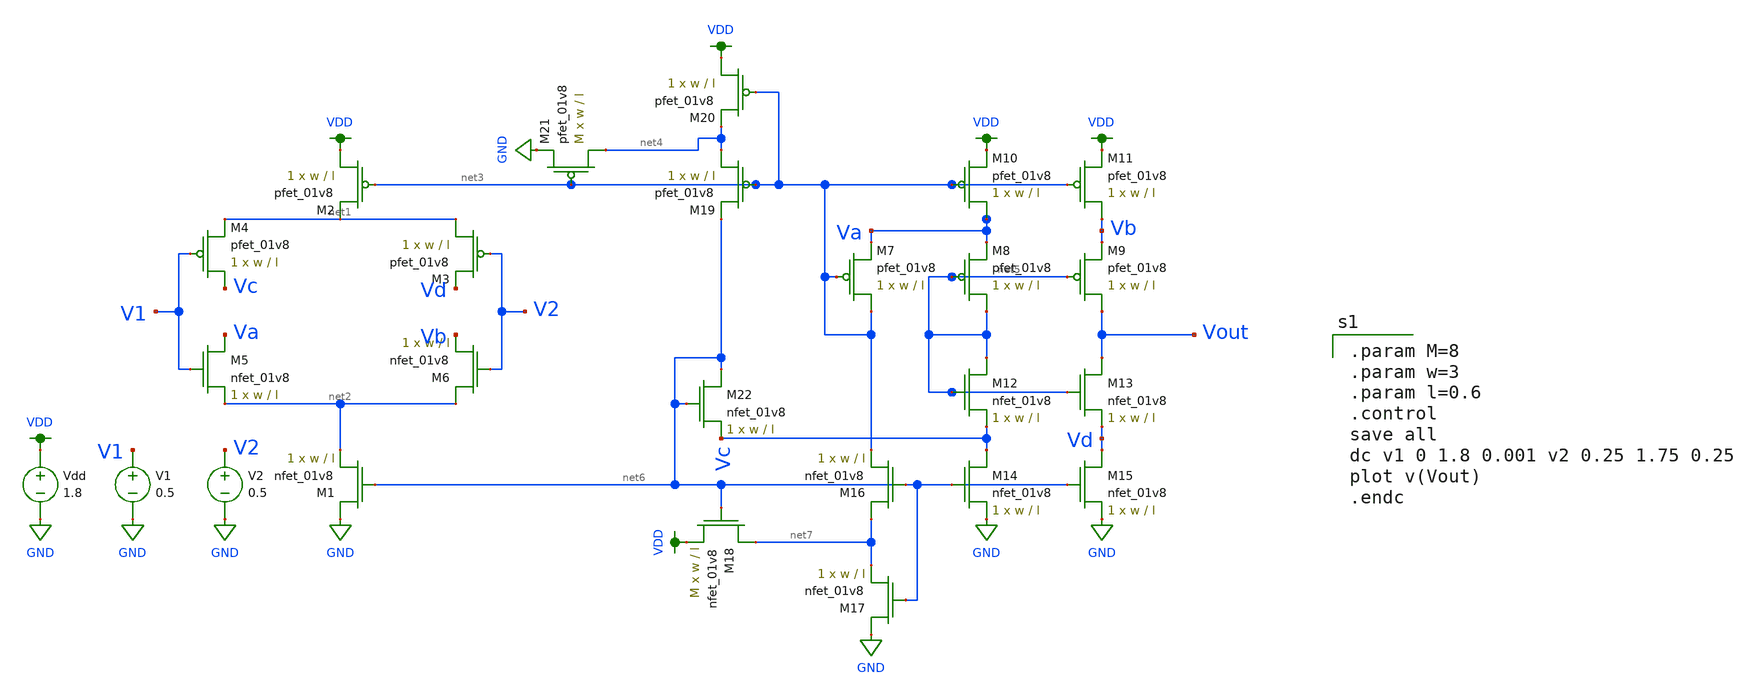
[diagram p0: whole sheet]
** sch_path: brad_circuit.sch
**.subckt brad_circuit
XM1 GND net6 net2 GND sky130_fd_pr__nfet_01v8 L=l W=w nf=1 ad='int((nf+1)/2) * W/nf * 0.29' as='int((nf+2)/2) * W/nf * 0.29'
+ pd='2*int((nf+1)/2) * (W/nf + 0.29)' ps='2*int((nf+2)/2) * (W/nf + 0.29)' nrd='0.29 / W' nrs='0.29 / W'
+ sa=0 sb=0 sd=0 mult=1 m=1
XM2 VDD net3 net1 VDD sky130_fd_pr__pfet_01v8 L=l W=w nf=1 ad='int((nf+1)/2) * W/nf * 0.29' as='int((nf+2)/2) * W/nf * 0.29'
+ pd='2*int((nf+1)/2) * (W/nf + 0.29)' ps='2*int((nf+2)/2) * (W/nf + 0.29)' nrd='0.29 / W' nrs='0.29 / W'
+ sa=0 sb=0 sd=0 mult=1 m=1
XM3 net1 V2 Vd VDD sky130_fd_pr__pfet_01v8 L=l W=w nf=1 ad='int((nf+1)/2) * W/nf * 0.29' as='int((nf+2)/2) * W/nf * 0.29'
+ pd='2*int((nf+1)/2) * (W/nf + 0.29)' ps='2*int((nf+2)/2) * (W/nf + 0.29)' nrd='0.29 / W' nrs='0.29 / W'
+ sa=0 sb=0 sd=0 mult=1 m=1
XM4 Vc V1 net1 VDD sky130_fd_pr__pfet_01v8 L=l W=w nf=1 ad='int((nf+1)/2) * W/nf * 0.29' as='int((nf+2)/2) * W/nf * 0.29'
+ pd='2*int((nf+1)/2) * (W/nf + 0.29)' ps='2*int((nf+2)/2) * (W/nf + 0.29)' nrd='0.29 / W' nrs='0.29 / W'
+ sa=0 sb=0 sd=0 mult=1 m=1
XM5 Va V1 net2 GND sky130_fd_pr__nfet_01v8 L=l W=w nf=1 ad='int((nf+1)/2) * W/nf * 0.29' as='int((nf+2)/2) * W/nf * 0.29'
+ pd='2*int((nf+1)/2) * (W/nf + 0.29)' ps='2*int((nf+2)/2) * (W/nf + 0.29)' nrd='0.29 / W' nrs='0.29 / W'
+ sa=0 sb=0 sd=0 mult=1 m=1
XM6 net2 V2 Vb GND sky130_fd_pr__nfet_01v8 L=l W=w nf=1 ad='int((nf+1)/2) * W/nf * 0.29' as='int((nf+2)/2) * W/nf * 0.29'
+ pd='2*int((nf+1)/2) * (W/nf + 0.29)' ps='2*int((nf+2)/2) * (W/nf + 0.29)' nrd='0.29 / W' nrs='0.29 / W'
+ sa=0 sb=0 sd=0 mult=1 m=1
XM7 net3 net3 Va VDD sky130_fd_pr__pfet_01v8 L=l W=w nf=1 ad='int((nf+1)/2) * W/nf * 0.29' as='int((nf+2)/2) * W/nf * 0.29'
+ pd='2*int((nf+1)/2) * (W/nf + 0.29)' ps='2*int((nf+2)/2) * (W/nf + 0.29)' nrd='0.29 / W' nrs='0.29 / W'
+ sa=0 sb=0 sd=0 mult=1 m=1
XM8 net5 net5 Va VDD sky130_fd_pr__pfet_01v8 L=l W=w nf=1 ad='int((nf+1)/2) * W/nf * 0.29' as='int((nf+2)/2) * W/nf * 0.29'
+ pd='2*int((nf+1)/2) * (W/nf + 0.29)' ps='2*int((nf+2)/2) * (W/nf + 0.29)' nrd='0.29 / W' nrs='0.29 / W'
+ sa=0 sb=0 sd=0 mult=1 m=1
XM9 Vout net5 Vb VDD sky130_fd_pr__pfet_01v8 L=l W=w nf=1 ad='int((nf+1)/2) * W/nf * 0.29' as='int((nf+2)/2) * W/nf * 0.29'
+ pd='2*int((nf+1)/2) * (W/nf + 0.29)' ps='2*int((nf+2)/2) * (W/nf + 0.29)' nrd='0.29 / W' nrs='0.29 / W'
+ sa=0 sb=0 sd=0 mult=1 m=1
XM10 Va net3 VDD VDD sky130_fd_pr__pfet_01v8 L=l W=w nf=1 ad='int((nf+1)/2) * W/nf * 0.29' as='int((nf+2)/2) * W/nf * 0.29'
+ pd='2*int((nf+1)/2) * (W/nf + 0.29)' ps='2*int((nf+2)/2) * (W/nf + 0.29)' nrd='0.29 / W' nrs='0.29 / W'
+ sa=0 sb=0 sd=0 mult=1 m=1
XM11 Vb net3 VDD VDD sky130_fd_pr__pfet_01v8 L=l W=w nf=1 ad='int((nf+1)/2) * W/nf * 0.29' as='int((nf+2)/2) * W/nf * 0.29'
+ pd='2*int((nf+1)/2) * (W/nf + 0.29)' ps='2*int((nf+2)/2) * (W/nf + 0.29)' nrd='0.29 / W' nrs='0.29 / W'
+ sa=0 sb=0 sd=0 mult=1 m=1
XM12 net5 net5 Vc GND sky130_fd_pr__nfet_01v8 L=l W=w nf=1 ad='int((nf+1)/2) * W/nf * 0.29' as='int((nf+2)/2) * W/nf * 0.29'
+ pd='2*int((nf+1)/2) * (W/nf + 0.29)' ps='2*int((nf+2)/2) * (W/nf + 0.29)' nrd='0.29 / W' nrs='0.29 / W'
+ sa=0 sb=0 sd=0 mult=1 m=1
XM13 Vout net5 Vd GND sky130_fd_pr__nfet_01v8 L=l W=w nf=1 ad='int((nf+1)/2) * W/nf * 0.29' as='int((nf+2)/2) * W/nf * 0.29'
+ pd='2*int((nf+1)/2) * (W/nf + 0.29)' ps='2*int((nf+2)/2) * (W/nf + 0.29)' nrd='0.29 / W' nrs='0.29 / W'
+ sa=0 sb=0 sd=0 mult=1 m=1
XM14 Vc net6 GND GND sky130_fd_pr__nfet_01v8 L=l W=w nf=1 ad='int((nf+1)/2) * W/nf * 0.29' as='int((nf+2)/2) * W/nf * 0.29'
+ pd='2*int((nf+1)/2) * (W/nf + 0.29)' ps='2*int((nf+2)/2) * (W/nf + 0.29)' nrd='0.29 / W' nrs='0.29 / W'
+ sa=0 sb=0 sd=0 mult=1 m=1
XM15 Vd net6 GND GND sky130_fd_pr__nfet_01v8 L=l W=w nf=1 ad='int((nf+1)/2) * W/nf * 0.29' as='int((nf+2)/2) * W/nf * 0.29'
+ pd='2*int((nf+1)/2) * (W/nf + 0.29)' ps='2*int((nf+2)/2) * (W/nf + 0.29)' nrd='0.29 / W' nrs='0.29 / W'
+ sa=0 sb=0 sd=0 mult=1 m=1
XM16 net7 net6 net3 GND sky130_fd_pr__nfet_01v8 L=l W=w nf=1 ad='int((nf+1)/2) * W/nf * 0.29' as='int((nf+2)/2) * W/nf * 0.29'
+ pd='2*int((nf+1)/2) * (W/nf + 0.29)' ps='2*int((nf+2)/2) * (W/nf + 0.29)' nrd='0.29 / W' nrs='0.29 / W'
+ sa=0 sb=0 sd=0 mult=1 m=1
XM17 GND net6 net7 GND sky130_fd_pr__nfet_01v8 L=l W=w nf=1 ad='int((nf+1)/2) * W/nf * 0.29' as='int((nf+2)/2) * W/nf * 0.29'
+ pd='2*int((nf+1)/2) * (W/nf + 0.29)' ps='2*int((nf+2)/2) * (W/nf + 0.29)' nrd='0.29 / W' nrs='0.29 / W'
+ sa=0 sb=0 sd=0 mult=1 m=1
XM18 net7 net6 VDD GND sky130_fd_pr__nfet_01v8 L=l W=w nf=1 ad='int((nf+1)/2) * W/nf * 0.29' as='int((nf+2)/2) * W/nf * 0.29'
+ pd='2*int((nf+1)/2) * (W/nf + 0.29)' ps='2*int((nf+2)/2) * (W/nf + 0.29)' nrd='0.29 / W' nrs='0.29 / W'
+ sa=0 sb=0 sd=0 mult=M m=M
XM19 net4 net3 net6 VDD sky130_fd_pr__pfet_01v8 L=l W=w nf=1 ad='int((nf+1)/2) * W/nf * 0.29' as='int((nf+2)/2) * W/nf * 0.29'
+ pd='2*int((nf+1)/2) * (W/nf + 0.29)' ps='2*int((nf+2)/2) * (W/nf + 0.29)' nrd='0.29 / W' nrs='0.29 / W'
+ sa=0 sb=0 sd=0 mult=1 m=1
XM20 VDD net3 net4 VDD sky130_fd_pr__pfet_01v8 L=l W=w nf=1 ad='int((nf+1)/2) * W/nf * 0.29' as='int((nf+2)/2) * W/nf * 0.29'
+ pd='2*int((nf+1)/2) * (W/nf + 0.29)' ps='2*int((nf+2)/2) * (W/nf + 0.29)' nrd='0.29 / W' nrs='0.29 / W'
+ sa=0 sb=0 sd=0 mult=1 m=1
XM21 net4 net3 GND VDD sky130_fd_pr__pfet_01v8 L=l W=w nf=1 ad='int((nf+1)/2) * W/nf * 0.29' as='int((nf+2)/2) * W/nf * 0.29'
+ pd='2*int((nf+1)/2) * (W/nf + 0.29)' ps='2*int((nf+2)/2) * (W/nf + 0.29)' nrd='0.29 / W' nrs='0.29 / W'
+ sa=0 sb=0 sd=0 mult=M m=M
XM22 net6 net6 Vc GND sky130_fd_pr__nfet_01v8 L=l W=w nf=1 ad='int((nf+1)/2) * W/nf * 0.29' as='int((nf+2)/2) * W/nf * 0.29'
+ pd='2*int((nf+1)/2) * (W/nf + 0.29)' ps='2*int((nf+2)/2) * (W/nf + 0.29)' nrd='0.29 / W' nrs='0.29 / W'
+ sa=0 sb=0 sd=0 mult=1 m=1
Vdd VDD GND 1.8
V1 V1 GND 0.5
V2 V2 GND 0.5
**** begin user architecture code

.option wnflag=1
.param MC_SWITCH=0.0
.lib ~/skywater/skywater-pdk/libraries/sky130_fd_pr_ngspice/latest/models/sky130.lib.spice tt


.param M=8
.param w=3
.param l=0.6
.control
save all
dc v1 0 1.8 0.001 v2 0.25 1.75 0.25
plot v(Vout)
.endc

**** end user architecture code
**.ends
.GLOBAL VDD
.GLOBAL GND
.end
